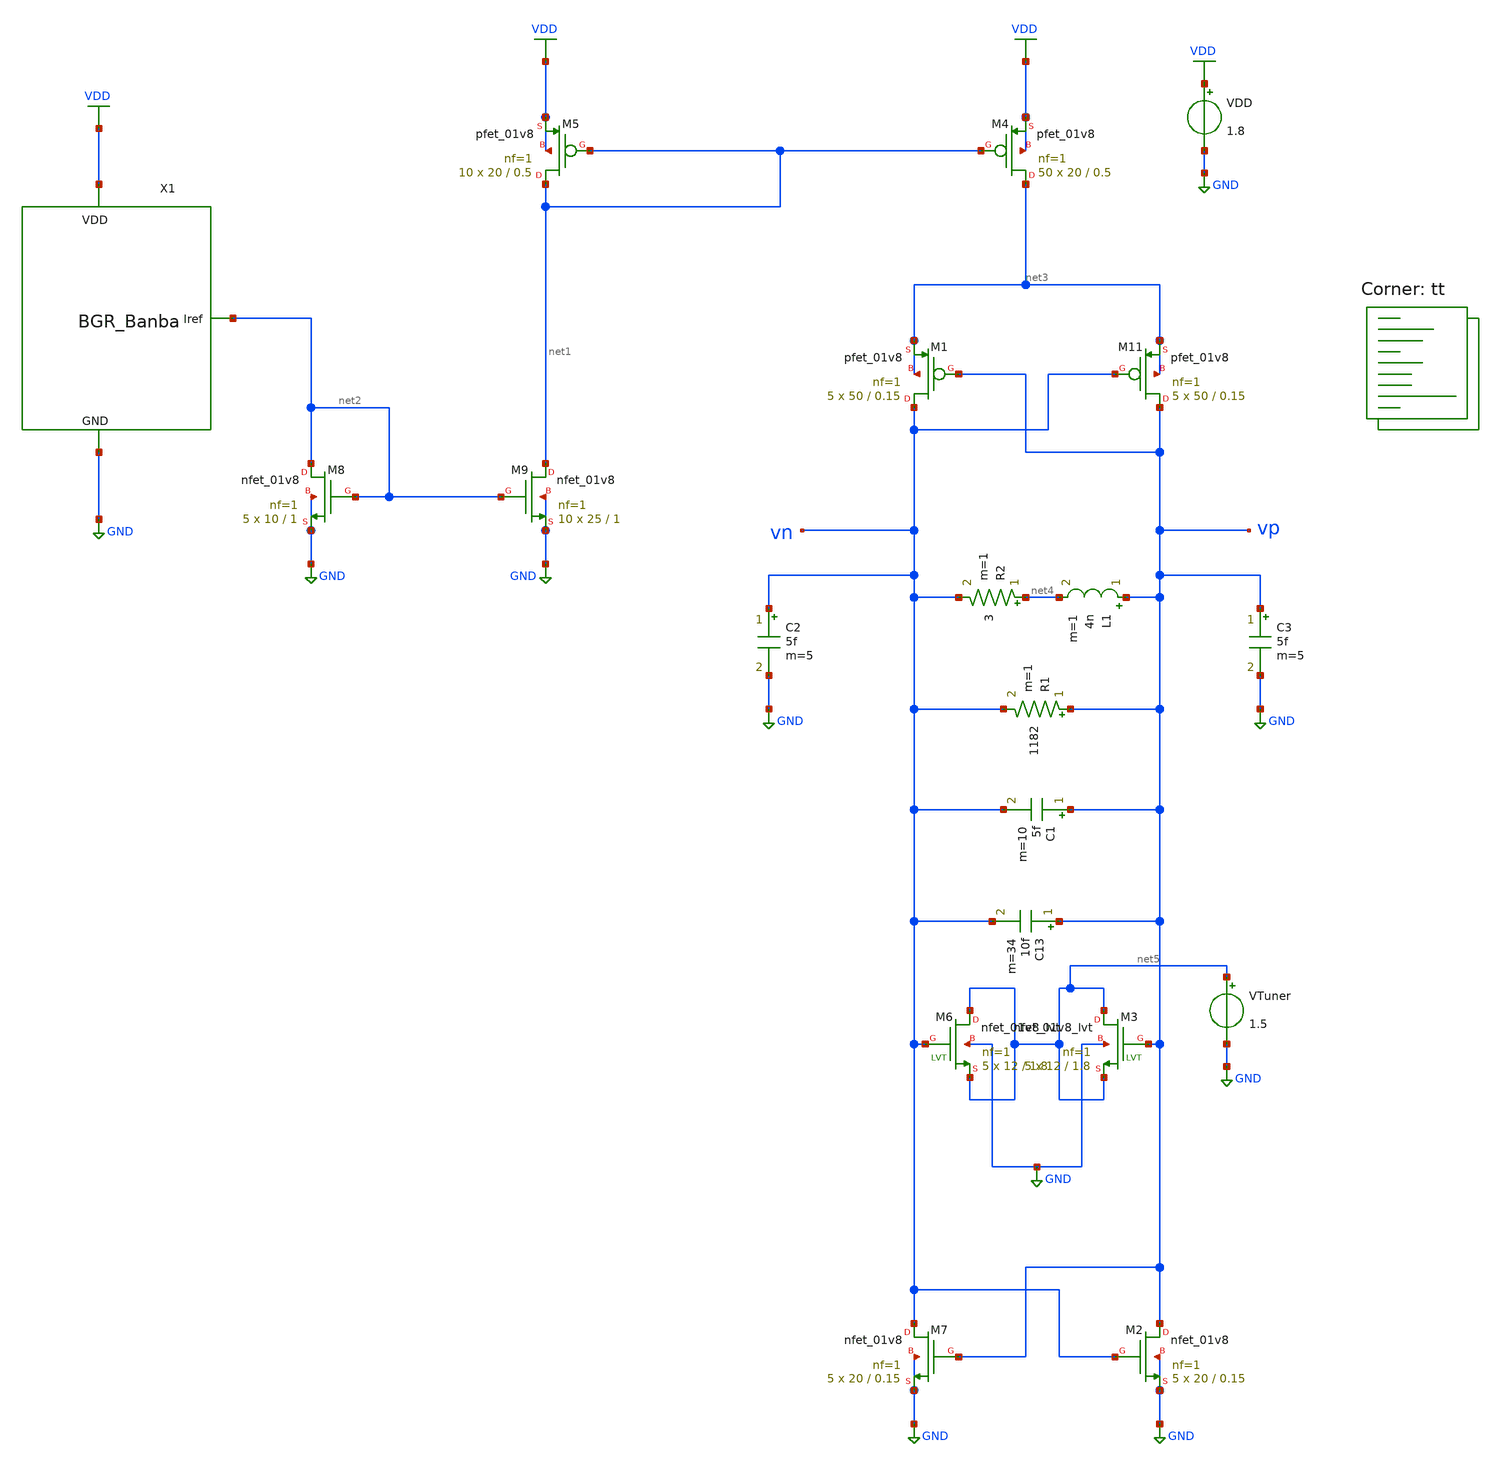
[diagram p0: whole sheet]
** sch_path: pll/lc_vco_lib_Ahmed_Reda/VCO_final/xschem/VCO_final.sch
**.subckt VCO_final
VDD VDD GND 1.8
X1 net2 GND VDD BGR_Banba
XM8 net2 net2 GND GND sky130_fd_pr__nfet_01v8 L=1 W=10 nf=1 ad='int((1 + 1)/2) * 10 / 1 * 0.29' as='int((1 + 2)/2) * 10 / 1 * 0.29'
+ pd='2*int((1 + 1)/2) * (10 / 1 + 0.29)' ps='2*int((1 + 2)/2) * (10 / 1 + 0.29)' nrd='0.29 / 10 ' nrs='0.29 / 10 '
+ sa=0 sb=0 sd=0 mult=5 m=5
XM9 net1 net2 GND GND sky130_fd_pr__nfet_01v8 L=1 W=25 nf=1 ad='int((1 + 1)/2) * 25 / 1 * 0.29' as='int((1 + 2)/2) * 25 / 1 * 0.29'
+ pd='2*int((1 + 1)/2) * (25 / 1 + 0.29)' ps='2*int((1 + 2)/2) * (25 / 1 + 0.29)' nrd='0.29 / 25 ' nrs='0.29 / 25 '
+ sa=0 sb=0 sd=0 mult=10 m=10
XM11 vp vn net3 net3 sky130_fd_pr__pfet_01v8 L=0.15 W=50 nf=1 ad='int((nf+1)/2) * W/nf * 0.29' as='int((nf+2)/2) * W/nf * 0.29'
+ pd='2*int((nf+1)/2) * (W/nf + 0.29)' ps='2*int((nf+2)/2) * (W/nf + 0.29)' nrd='0.29 / W' nrs='0.29 / W'
+ sa=0 sb=0 sd=0 mult=5 m=5
XM1 vn vp net3 net3 sky130_fd_pr__pfet_01v8 L=0.15 W=50 nf=1 ad='int((nf+1)/2) * W/nf * 0.29' as='int((nf+2)/2) * W/nf * 0.29'
+ pd='2*int((nf+1)/2) * (W/nf + 0.29)' ps='2*int((nf+2)/2) * (W/nf + 0.29)' nrd='0.29 / W' nrs='0.29 / W'
+ sa=0 sb=0 sd=0 mult=5 m=5
XM2 vp vn GND GND sky130_fd_pr__nfet_01v8 L=0.15 W=20 nf=1 ad='int((1 + 1)/2) * 20 / 1 * 0.29' as='int((1 + 2)/2) * 20 / 1 * 0.29'
+ pd='2*int((1 + 1)/2) * (20 / 1 + 0.29)' ps='2*int((1 + 2)/2) * (20 / 1 + 0.29)' nrd='0.29 / 20 ' nrs='0.29 / 20 '
+ sa=0 sb=0 sd=0 mult=5 m=5
L1 vp net4 4n m=1
R1 vp vn 1182 m=1
R2 net4 vn 3 m=1
XM7 vn vp GND GND sky130_fd_pr__nfet_01v8 L=0.15 W=20 nf=1 ad='int((1 + 1)/2) * 20 / 1 * 0.29' as='int((1 + 2)/2) * 20 / 1 * 0.29'
+ pd='2*int((1 + 1)/2) * (20 / 1 + 0.29)' ps='2*int((1 + 2)/2) * (20 / 1 + 0.29)' nrd='0.29 / 20 ' nrs='0.29 / 20 '
+ sa=0 sb=0 sd=0 mult=5 m=5
C1 vp vn 5f m=10
C3 vp GND 5f m=5
C2 vn GND 5f m=5
VTuner net5 GND 1.5
C13 vp vn 10f m=34
XM6 net5 vn net5 GND sky130_fd_pr__nfet_01v8_lvt L=1.8 W=12 nf=1 ad='int((1 + 1)/2) * 12 / 1 * 0.29'
+ as='int((1 + 2)/2) * 12 / 1 * 0.29' pd='2*int((1 + 1)/2) * (12 / 1 + 0.29)' ps='2*int((1 + 2)/2) * (12 / 1 + 0.29)'
+ nrd='0.29 / 12 ' nrs='0.29 / 12 ' sa=0 sb=0 sd=0 mult=5 m=5
XM3 net5 vp net5 GND sky130_fd_pr__nfet_01v8_lvt L=1.8 W=12 nf=1 ad='int((1 + 1)/2) * 12 / 1 * 0.29'
+ as='int((1 + 2)/2) * 12 / 1 * 0.29' pd='2*int((1 + 1)/2) * (12 / 1 + 0.29)' ps='2*int((1 + 2)/2) * (12 / 1 + 0.29)'
+ nrd='0.29 / 12 ' nrs='0.29 / 12 ' sa=0 sb=0 sd=0 mult=5 m=5
XM4 net3 net1 VDD VDD sky130_fd_pr__pfet_01v8 L=0.5 W=20 nf=1 ad='int((nf+1)/2) * W/nf * 0.29' as='int((nf+2)/2) * W/nf * 0.29'
+ pd='2*int((nf+1)/2) * (W/nf + 0.29)' ps='2*int((nf+2)/2) * (W/nf + 0.29)' nrd='0.29 / W' nrs='0.29 / W'
+ sa=0 sb=0 sd=0 mult=50 m=50
XM5 net1 net1 VDD VDD sky130_fd_pr__pfet_01v8 L=0.5 W=20 nf=1 ad='int((nf+1)/2) * W/nf * 0.29' as='int((nf+2)/2) * W/nf * 0.29'
+ pd='2*int((nf+1)/2) * (W/nf + 0.29)' ps='2*int((nf+2)/2) * (W/nf + 0.29)' nrd='0.29 / W' nrs='0.29 / W'
+ sa=0 sb=0 sd=0 mult=10 m=10
**** begin user architecture code
.lib $::SKYWATER_MODELS/sky130.lib.spice tt


.save all
.nodeset v(vout)=0
.control
compose  vctrl_vector   start=0         stop=1.6          step=0.05
let vctrl_counter = 0
let f_osc = vector(length(vctrl_vector))
let curr_value = vctrl_vector[0]
set appendwrite
while vctrl_counter < length(vctrl_vector)
    print curr_value
    alter VTuner  $&curr_value
    tran 0.01ns 100ns
    let vdiff = v(vp)-v(vn)
    meas tran tperiod TRIG vdiff VAL=0.5 RISE=30 TARG vdiff VAL=0.5 RISE=31
    let freq = 1/tperiod
    setplot op1
    let f_osc[vctrl_counter] = tran.freq
    *wrdata fosc_vs_vctrl.csv f_osc[vctrl_counter]
    reset
    let vctrl_counter = vctrl_counter + 1
    let curr_value = vctrl_vector[vctrl_counter]
end

let kvco = vecd(f_osc)
write output.txt f_osc
print f_osc
plot f_osc vs vctrl_vector
*plot kvco vs vctrl_vector xlimit 0.5 1.6
*print kvco
.endc


**** end user architecture code
**.ends
.GLOBAL GND
.GLOBAL VDD
.end
